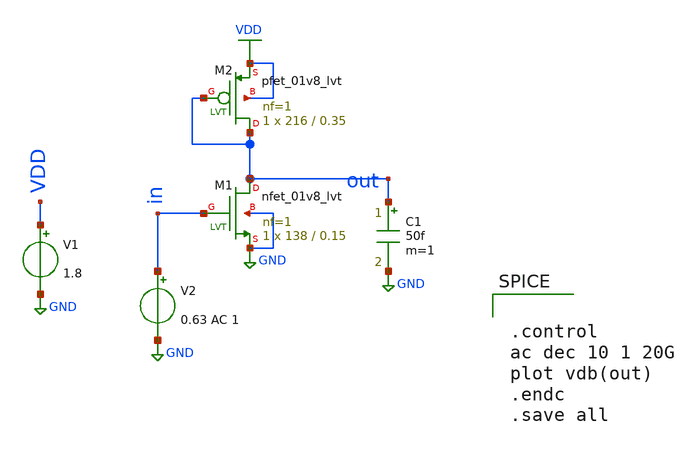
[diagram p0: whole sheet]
** sch_path: #4_amplifier_diodeConnected/d4.sch
**.subckt d4
V1 VDD GND 1.8
V2 in GND 0.63 AC 1
C1 out GND 50f m=1
XM1 out in GND GND sky130_fd_pr__nfet_01v8_lvt L=0.15 W=138 nf=1 ad='int((nf+1)/2) * W/nf * 0.29' as='int((nf+2)/2) * W/nf * 0.29'
+ pd='2*int((nf+1)/2) * (W/nf + 0.29)' ps='2*int((nf+2)/2) * (W/nf + 0.29)' nrd='0.29 / W' nrs='0.29 / W'
+ sa=0 sb=0 sd=0 mult=1 m=1
XM2 out out VDD VDD sky130_fd_pr__pfet_01v8_lvt L=0.35 W=216 nf=1 ad='int((nf+1)/2) * W/nf * 0.29' as='int((nf+2)/2) * W/nf * 0.29'
+ pd='2*int((nf+1)/2) * (W/nf + 0.29)' ps='2*int((nf+2)/2) * (W/nf + 0.29)' nrd='0.29 / W' nrs='0.29 / W'
+ sa=0 sb=0 sd=0 mult=1 m=1
**** begin user architecture code

** opencircuitdesign pdks install
.lib $::SKYWATER_MODELS/sky130.lib.spice tt




.control
ac dec 10 1 20G
plot vdb(out)
.endc
.save all


**** end user architecture code
**.ends
.GLOBAL GND
.GLOBAL VDD
.end
